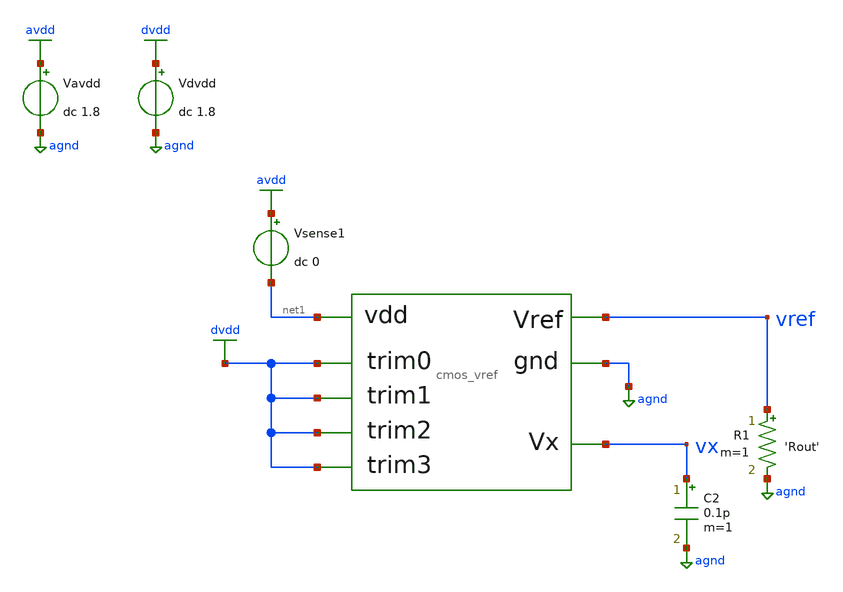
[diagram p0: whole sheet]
** sch_path: xschem/cmos_vref_output_tb.sch
**.subckt cmos_vref_output_tb
Vavdd avdd agnd dc 1.8
X1 net1 agnd dvdd vref vx dvdd dvdd dvdd cmos_vref
Vsense1 avdd net1 dc 0
C2 vx agnd 0.1p m=1
Vdvdd dvdd agnd dc 1.8
R1 vref agnd 'Rout' m=1
**** begin user architecture code


.control
dc TEMP -50 140 5
save all
write tb_gain.raw
.endc




.option TRTOL=5
.option SCALE=1e-6

.param vref_m1width=3
.param vref_m1length=40
.param vref_m1fingers=1
.param vref_m2width=3
.param vref_m2length=20
.param vref_m2fingers=1
.param vref_m3width=720
.param vref_m3length=2
.param vref_m3fingers=24
.param vref_m4width=60
.param vref_m4length=2
.param vref_m4fingers=4
.param vref_m56width=20
.param vref_m56length=20
.param vref_m56fingers=1
.param vref_m78width=50
.param vref_m78length=20
.param vref_m78fingers=5
.param vref_m9width=100
.param vref_m789length=20




.lib /usr/local/share/pdk/sky130A/libs.tech/combined/sky130.lib.spice tt

**** end user architecture code
**.ends

* expanding   symbol:  /home/moduhub/work/sky130_ak_ip__cmos_vref/xschem/cmos_vref.sym # of pins=8
** sym_path: xschem/cmos_vref.sym
** sch_path: xschem/cmos_vref.sch
.subckt cmos_vref vdd gnd trim0 vref vx trim1 trim2 trim3
*.opin vref
*.iopin gnd
*.iopin vdd
*.opin vx
*.ipin trim0
*.ipin trim1
*.ipin trim2
*.ipin trim3
XM2 vref vref vx GND sky130_fd_pr__nfet_01v8 L=10 W=2 nf=1 ad='int((nf+1)/2) * W/nf * 0.29' as='int((nf+2)/2) * W/nf * 0.29'
+ pd='2*int((nf+1)/2) * (W/nf + 0.29)' ps='2*int((nf+2)/2) * (W/nf + 0.29)' nrd='0.29 / W' nrs='0.29 / W'
+ sa=0 sb=0 sd=0 mult=1 m=1
XM1 vx vref gnd GND sky130_fd_pr__nfet_01v8 L=20 W=2 nf=1 ad='int((nf+1)/2) * W/nf * 0.29' as='int((nf+2)/2) * W/nf * 0.29'
+ pd='2*int((nf+1)/2) * (W/nf + 0.29)' ps='2*int((nf+2)/2) * (W/nf + 0.29)' nrd='0.29 / W' nrs='0.29 / W'
+ sa=0 sb=0 sd=0 mult=1 m=1
XM3 net1 net3 vx GND sky130_fd_pr__nfet_01v8 L=1 W=100 nf=5 ad='int((nf+1)/2) * W/nf * 0.29' as='int((nf+2)/2) * W/nf * 0.29'
+ pd='2*int((nf+1)/2) * (W/nf + 0.29)' ps='2*int((nf+2)/2) * (W/nf + 0.29)' nrd='0.29 / W' nrs='0.29 / W'
+ sa=0 sb=0 sd=0 mult=1 m=1
XM4 net2 net3 gnd GND sky130_fd_pr__nfet_01v8 L=1 W=5 nf=1 ad='int((nf+1)/2) * W/nf * 0.29' as='int((nf+2)/2) * W/nf * 0.29'
+ pd='2*int((nf+1)/2) * (W/nf + 0.29)' ps='2*int((nf+2)/2) * (W/nf + 0.29)' nrd='0.29 / W' nrs='0.29 / W'
+ sa=0 sb=0 sd=0 mult=1 m=1
XM5 net4 vref net1 GND sky130_fd_pr__nfet_01v8 L=10 W=10 nf=1 ad='int((nf+1)/2) * W/nf * 0.29' as='int((nf+2)/2) * W/nf * 0.29'
+ pd='2*int((nf+1)/2) * (W/nf + 0.29)' ps='2*int((nf+2)/2) * (W/nf + 0.29)' nrd='0.29 / W' nrs='0.29 / W'
+ sa=0 sb=0 sd=0 mult=1 m=1
XM6 net3 vref net2 GND sky130_fd_pr__nfet_01v8 L=10 W=10 nf=1 ad='int((nf+1)/2) * W/nf * 0.29' as='int((nf+2)/2) * W/nf * 0.29'
+ pd='2*int((nf+1)/2) * (W/nf + 0.29)' ps='2*int((nf+2)/2) * (W/nf + 0.29)' nrd='0.29 / W' nrs='0.29 / W'
+ sa=0 sb=0 sd=0 mult=1 m=1
XM7 net4 net4 vdd VDD sky130_fd_pr__pfet_01v8 L=10 W=5 nf=1 ad='int((nf+1)/2) * W/nf * 0.29' as='int((nf+2)/2) * W/nf * 0.29'
+ pd='2*int((nf+1)/2) * (W/nf + 0.29)' ps='2*int((nf+2)/2) * (W/nf + 0.29)' nrd='0.29 / W' nrs='0.29 / W'
+ sa=0 sb=0 sd=0 mult=1 m=1
XM8 net3 net4 vdd VDD sky130_fd_pr__pfet_01v8 L=10 W=5 nf=1 ad='int((nf+1)/2) * W/nf * 0.29' as='int((nf+2)/2) * W/nf * 0.29'
+ pd='2*int((nf+1)/2) * (W/nf + 0.29)' ps='2*int((nf+2)/2) * (W/nf + 0.29)' nrd='0.29 / W' nrs='0.29 / W'
+ sa=0 sb=0 sd=0 mult=1 m=1
XM9 vref net4 vdd VDD sky130_fd_pr__pfet_01v8 L=10 W=50 nf=1 ad='int((nf+1)/2) * W/nf * 0.29' as='int((nf+2)/2) * W/nf * 0.29'
+ pd='2*int((nf+1)/2) * (W/nf + 0.29)' ps='2*int((nf+2)/2) * (W/nf + 0.29)' nrd='0.29 / W' nrs='0.29 / W'
+ sa=0 sb=0 sd=0 mult=1 m=1
XM10 net5 net3 gnd GND sky130_fd_pr__nfet_01v8 L=0.15 W=1 nf=1 ad='int((nf+1)/2) * W/nf * 0.29' as='int((nf+2)/2) * W/nf * 0.29'
+ pd='2*int((nf+1)/2) * (W/nf + 0.29)' ps='2*int((nf+2)/2) * (W/nf + 0.29)' nrd='0.29 / W' nrs='0.29 / W'
+ sa=0 sb=0 sd=0 mult=1 m=1
XM11 net4 net5 gnd GND sky130_fd_pr__nfet_01v8 L=0.15 W=1 nf=1 ad='int((nf+1)/2) * W/nf * 0.29' as='int((nf+2)/2) * W/nf * 0.29'
+ pd='2*int((nf+1)/2) * (W/nf + 0.29)' ps='2*int((nf+2)/2) * (W/nf + 0.29)' nrd='0.29 / W' nrs='0.29 / W'
+ sa=0 sb=0 sd=0 mult=1 m=1
XC1 vdd net5 sky130_fd_pr__cap_mim_m3_1 W=1 L=1 MF=1 m=1
XM12 vref net4 net9 VDD sky130_fd_pr__pfet_01v8 L=0.15 W=1 nf=1 ad='int((nf+1)/2) * W/nf * 0.29' as='int((nf+2)/2) * W/nf * 0.29'
+ pd='2*int((nf+1)/2) * (W/nf + 0.29)' ps='2*int((nf+2)/2) * (W/nf + 0.29)' nrd='0.29 / W' nrs='0.29 / W'
+ sa=0 sb=0 sd=0 mult=1 m=1
XM13 vref net4 net8 VDD sky130_fd_pr__pfet_01v8 L=0.15 W=1 nf=1 ad='int((nf+1)/2) * W/nf * 0.29' as='int((nf+2)/2) * W/nf * 0.29'
+ pd='2*int((nf+1)/2) * (W/nf + 0.29)' ps='2*int((nf+2)/2) * (W/nf + 0.29)' nrd='0.29 / W' nrs='0.29 / W'
+ sa=0 sb=0 sd=0 mult=1 m=1
XM14 net9 trim0 vdd VDD sky130_fd_pr__pfet_01v8 L=0.15 W=1 nf=1 ad='int((nf+1)/2) * W/nf * 0.29' as='int((nf+2)/2) * W/nf * 0.29'
+ pd='2*int((nf+1)/2) * (W/nf + 0.29)' ps='2*int((nf+2)/2) * (W/nf + 0.29)' nrd='0.29 / W' nrs='0.29 / W'
+ sa=0 sb=0 sd=0 mult=1 m=1
XM15 net8 trim1 vdd VDD sky130_fd_pr__pfet_01v8 L=0.15 W=1 nf=1 ad='int((nf+1)/2) * W/nf * 0.29' as='int((nf+2)/2) * W/nf * 0.29'
+ pd='2*int((nf+1)/2) * (W/nf + 0.29)' ps='2*int((nf+2)/2) * (W/nf + 0.29)' nrd='0.29 / W' nrs='0.29 / W'
+ sa=0 sb=0 sd=0 mult=1 m=1
XM16 vref net4 net7 VDD sky130_fd_pr__pfet_01v8 L=0.15 W=1 nf=1 ad='int((nf+1)/2) * W/nf * 0.29' as='int((nf+2)/2) * W/nf * 0.29'
+ pd='2*int((nf+1)/2) * (W/nf + 0.29)' ps='2*int((nf+2)/2) * (W/nf + 0.29)' nrd='0.29 / W' nrs='0.29 / W'
+ sa=0 sb=0 sd=0 mult=1 m=1
XM17 net7 trim2 vdd VDD sky130_fd_pr__pfet_01v8 L=0.15 W=1 nf=1 ad='int((nf+1)/2) * W/nf * 0.29' as='int((nf+2)/2) * W/nf * 0.29'
+ pd='2*int((nf+1)/2) * (W/nf + 0.29)' ps='2*int((nf+2)/2) * (W/nf + 0.29)' nrd='0.29 / W' nrs='0.29 / W'
+ sa=0 sb=0 sd=0 mult=1 m=1
XM18 vref net4 net6 VDD sky130_fd_pr__pfet_01v8 L=0.15 W=1 nf=1 ad='int((nf+1)/2) * W/nf * 0.29' as='int((nf+2)/2) * W/nf * 0.29'
+ pd='2*int((nf+1)/2) * (W/nf + 0.29)' ps='2*int((nf+2)/2) * (W/nf + 0.29)' nrd='0.29 / W' nrs='0.29 / W'
+ sa=0 sb=0 sd=0 mult=1 m=1
XM19 net6 trim3 vdd VDD sky130_fd_pr__pfet_01v8 L=0.15 W=1 nf=1 ad='int((nf+1)/2) * W/nf * 0.29' as='int((nf+2)/2) * W/nf * 0.29'
+ pd='2*int((nf+1)/2) * (W/nf + 0.29)' ps='2*int((nf+2)/2) * (W/nf + 0.29)' nrd='0.29 / W' nrs='0.29 / W'
+ sa=0 sb=0 sd=0 mult=1 m=1
.ends

.GLOBAL avdd
.GLOBAL agnd
.GLOBAL dvdd
.end
